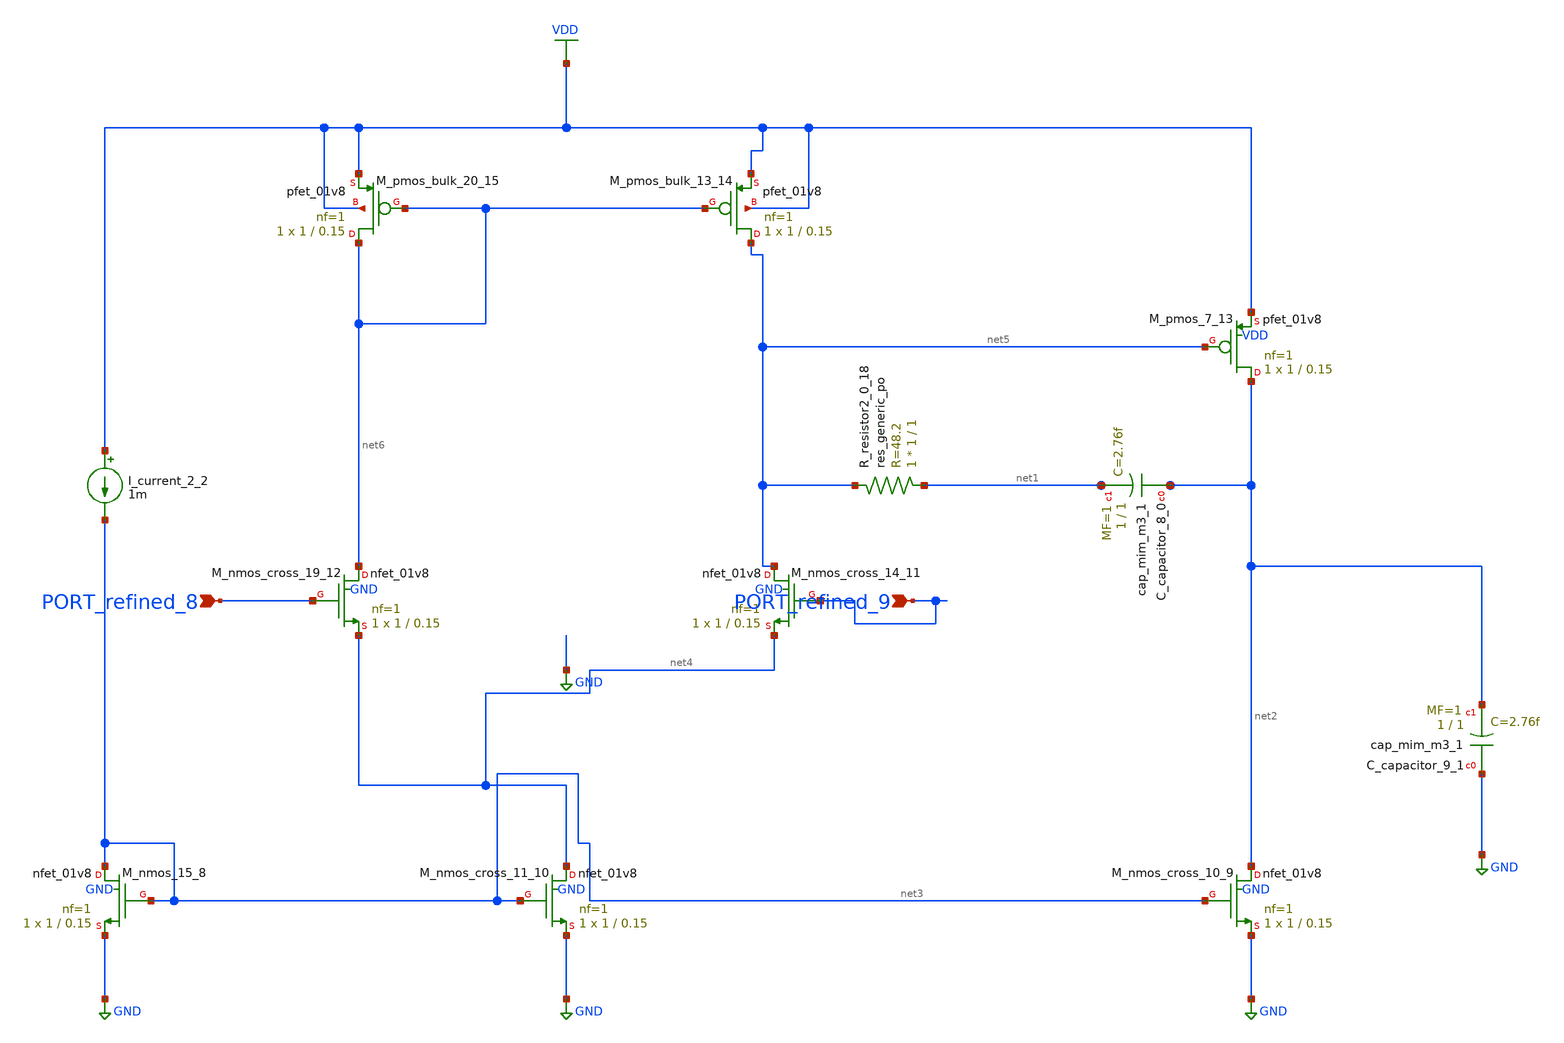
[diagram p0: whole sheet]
** sch_path: schematics/Image2Net/109.sch
**.subckt 109 PORT_refined_8 PORT_refined_9
*.ipin PORT_refined_8
*.ipin PORT_refined_9
XC_capacitor_8_0 net2 net1 sky130_fd_pr__cap_mim_m3_1 W=1 L=1 MF=1 m=1
XC_capacitor_9_1 GND net2 sky130_fd_pr__cap_mim_m3_1 W=1 L=1 MF=1 m=1
I_current_2_2 VDD net3 1m
XM_nmos_15_8 net3 net3 GND GND sky130_fd_pr__nfet_01v8 L=0.15 W=1 nf=1 ad='int((1 + 1)/2) * 1 / 1 * 0.29'
+ as='int((1 + 2)/2) * 1 / 1 * 0.29' pd='2*int((1 + 1)/2) * (1 / 1 + 0.29)' ps='2*int((1 + 2)/2) * (1 / 1 + 0.29)'
+ nrd='0.29 / 1 ' nrs='0.29 / 1 ' sa=0 sb=0 sd=0 mult=1 m=1
XM_nmos_cross_10_9 net2 net3 GND GND sky130_fd_pr__nfet_01v8 L=0.15 W=1 nf=1 ad='int((1 + 1)/2) * 1 / 1 * 0.29'
+ as='int((1 + 2)/2) * 1 / 1 * 0.29' pd='2*int((1 + 1)/2) * (1 / 1 + 0.29)' ps='2*int((1 + 2)/2) * (1 / 1 + 0.29)'
+ nrd='0.29 / 1 ' nrs='0.29 / 1 ' sa=0 sb=0 sd=0 mult=1 m=1
XM_nmos_cross_11_10 net4 net3 GND GND sky130_fd_pr__nfet_01v8 L=0.15 W=1 nf=1 ad='int((1 + 1)/2) * 1 / 1 * 0.29'
+ as='int((1 + 2)/2) * 1 / 1 * 0.29' pd='2*int((1 + 1)/2) * (1 / 1 + 0.29)' ps='2*int((1 + 2)/2) * (1 / 1 + 0.29)'
+ nrd='0.29 / 1 ' nrs='0.29 / 1 ' sa=0 sb=0 sd=0 mult=1 m=1
XM_nmos_cross_14_11 net5 PORT_refined_9 net4 GND sky130_fd_pr__nfet_01v8 L=0.15 W=1 nf=1 ad='int((1 + 1)/2) * 1 / 1 * 0.29'
+ as='int((1 + 2)/2) * 1 / 1 * 0.29' pd='2*int((1 + 1)/2) * (1 / 1 + 0.29)' ps='2*int((1 + 2)/2) * (1 / 1 + 0.29)'
+ nrd='0.29 / 1 ' nrs='0.29 / 1 ' sa=0 sb=0 sd=0 mult=1 m=1
XM_nmos_cross_19_12 net6 PORT_refined_8 net4 GND sky130_fd_pr__nfet_01v8 L=0.15 W=1 nf=1 ad='int((1 + 1)/2) * 1 / 1 * 0.29'
+ as='int((1 + 2)/2) * 1 / 1 * 0.29' pd='2*int((1 + 1)/2) * (1 / 1 + 0.29)' ps='2*int((1 + 2)/2) * (1 / 1 + 0.29)'
+ nrd='0.29 / 1 ' nrs='0.29 / 1 ' sa=0 sb=0 sd=0 mult=1 m=1
XM_pmos_7_13 net2 net5 VDD VDD sky130_fd_pr__pfet_01v8 L=0.15 W=1 nf=1 ad='int((1 + 1)/2) * 1 / 1 * 0.29'
+ as='int((1 + 2)/2) * 1 / 1 * 0.29' pd='2*int((1 + 1)/2) * (1 / 1 + 0.29)' ps='2*int((1 + 2)/2) * (1 / 1 + 0.29)'
+ nrd='0.29 / 1 ' nrs='0.29 / 1 ' sa=0 sb=0 sd=0 mult=1 m=1
XM_pmos_bulk_13_14 net5 net6 VDD VDD sky130_fd_pr__pfet_01v8 L=0.15 W=1 nf=1 ad='int((1 + 1)/2) * 1 / 1 * 0.29'
+ as='int((1 + 2)/2) * 1 / 1 * 0.29' pd='2*int((1 + 1)/2) * (1 / 1 + 0.29)' ps='2*int((1 + 2)/2) * (1 / 1 + 0.29)'
+ nrd='0.29 / 1 ' nrs='0.29 / 1 ' sa=0 sb=0 sd=0 mult=1 m=1
XM_pmos_bulk_20_15 net6 net6 VDD VDD sky130_fd_pr__pfet_01v8 L=0.15 W=1 nf=1 ad='int((1 + 1)/2) * 1 / 1 * 0.29'
+ as='int((1 + 2)/2) * 1 / 1 * 0.29' pd='2*int((1 + 1)/2) * (1 / 1 + 0.29)' ps='2*int((1 + 2)/2) * (1 / 1 + 0.29)'
+ nrd='0.29 / 1 ' nrs='0.29 / 1 ' sa=0 sb=0 sd=0 mult=1 m=1
XR_resistor2_0_18 net1 net5 sky130_fd_pr__res_generic_po W=1 L=1 m=1
**.ends
.GLOBAL GND
.GLOBAL VDD
.end
